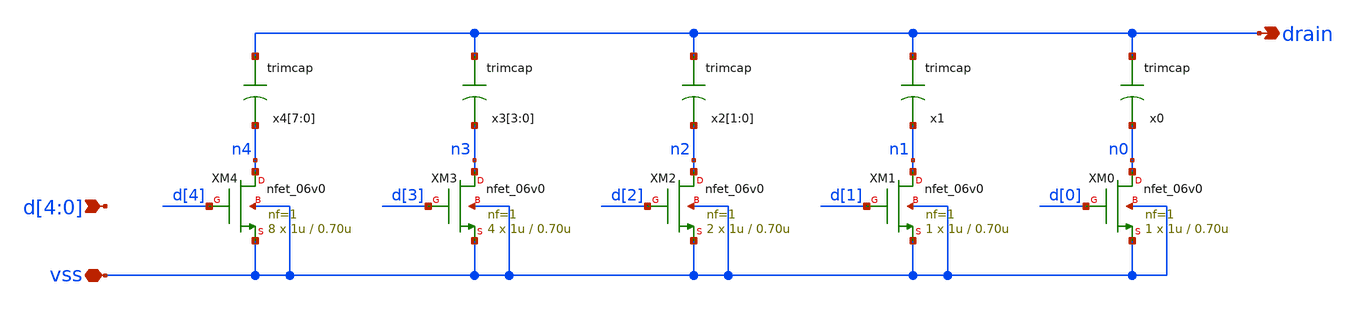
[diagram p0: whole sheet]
** sch_path: check/xschem/sar_10b/comparator/trim.sch
**.subckt trim vss d[4],d[3],d[2],d[1],d[0] drain
*.iopin vss
*.ipin d[4],d[3],d[2],d[1],d[0]
*.opin drain
x4[7] drain n4 trimcap
x4[6] drain n4 trimcap
x4[5] drain n4 trimcap
x4[4] drain n4 trimcap
x4[3] drain n4 trimcap
x4[2] drain n4 trimcap
x4[1] drain n4 trimcap
x4[0] drain n4 trimcap
x3[3] drain n3 trimcap
x3[2] drain n3 trimcap
x3[1] drain n3 trimcap
x3[0] drain n3 trimcap
x2[1] drain n2 trimcap
x2[0] drain n2 trimcap
x1 drain n1 trimcap
x0 drain n0 trimcap
XM0 n0 d[0] vss vss nfet_06v0 L=0.70u W=1u nf=1 ad='int((nf+1)/2) * W/nf * 0.18u' as='int((nf+2)/2) * W/nf * 0.18u'
+ pd='2*int((nf+1)/2) * (W/nf + 0.18u)' ps='2*int((nf+2)/2) * (W/nf + 0.18u)' nrd='0.18u / W' nrs='0.18u / W'
+ sa=0 sb=0 sd=0 m=1
XM1 n1 d[1] vss vss nfet_06v0 L=0.70u W=1u nf=1 ad='int((nf+1)/2) * W/nf * 0.18u' as='int((nf+2)/2) * W/nf * 0.18u'
+ pd='2*int((nf+1)/2) * (W/nf + 0.18u)' ps='2*int((nf+2)/2) * (W/nf + 0.18u)' nrd='0.18u / W' nrs='0.18u / W'
+ sa=0 sb=0 sd=0 m=1
XM2 n2 d[2] vss vss nfet_06v0 L=0.70u W=1u nf=1 ad='int((nf+1)/2) * W/nf * 0.18u' as='int((nf+2)/2) * W/nf * 0.18u'
+ pd='2*int((nf+1)/2) * (W/nf + 0.18u)' ps='2*int((nf+2)/2) * (W/nf + 0.18u)' nrd='0.18u / W' nrs='0.18u / W'
+ sa=0 sb=0 sd=0 m=2
XM3 n3 d[3] vss vss nfet_06v0 L=0.70u W=1u nf=1 ad='int((nf+1)/2) * W/nf * 0.18u' as='int((nf+2)/2) * W/nf * 0.18u'
+ pd='2*int((nf+1)/2) * (W/nf + 0.18u)' ps='2*int((nf+2)/2) * (W/nf + 0.18u)' nrd='0.18u / W' nrs='0.18u / W'
+ sa=0 sb=0 sd=0 m=4
XM4 n4 d[4] vss vss nfet_06v0 L=0.70u W=1u nf=1 ad='int((nf+1)/2) * W/nf * 0.18u' as='int((nf+2)/2) * W/nf * 0.18u'
+ pd='2*int((nf+1)/2) * (W/nf + 0.18u)' ps='2*int((nf+2)/2) * (W/nf + 0.18u)' nrd='0.18u / W' nrs='0.18u / W'
+ sa=0 sb=0 sd=0 m=8
**.ends

* expanding   symbol:  sar_10b/comparator/trimcap.sym # of pins=2
** sym_path: sar_10b/comparator/trimcap.sym
** sch_path: sar_10b/comparator/trimcap.sch
.subckt trimcap cp cn
*.iopin cp
*.iopin cn
c0 cp cn 1f m=1
.ends

.end
